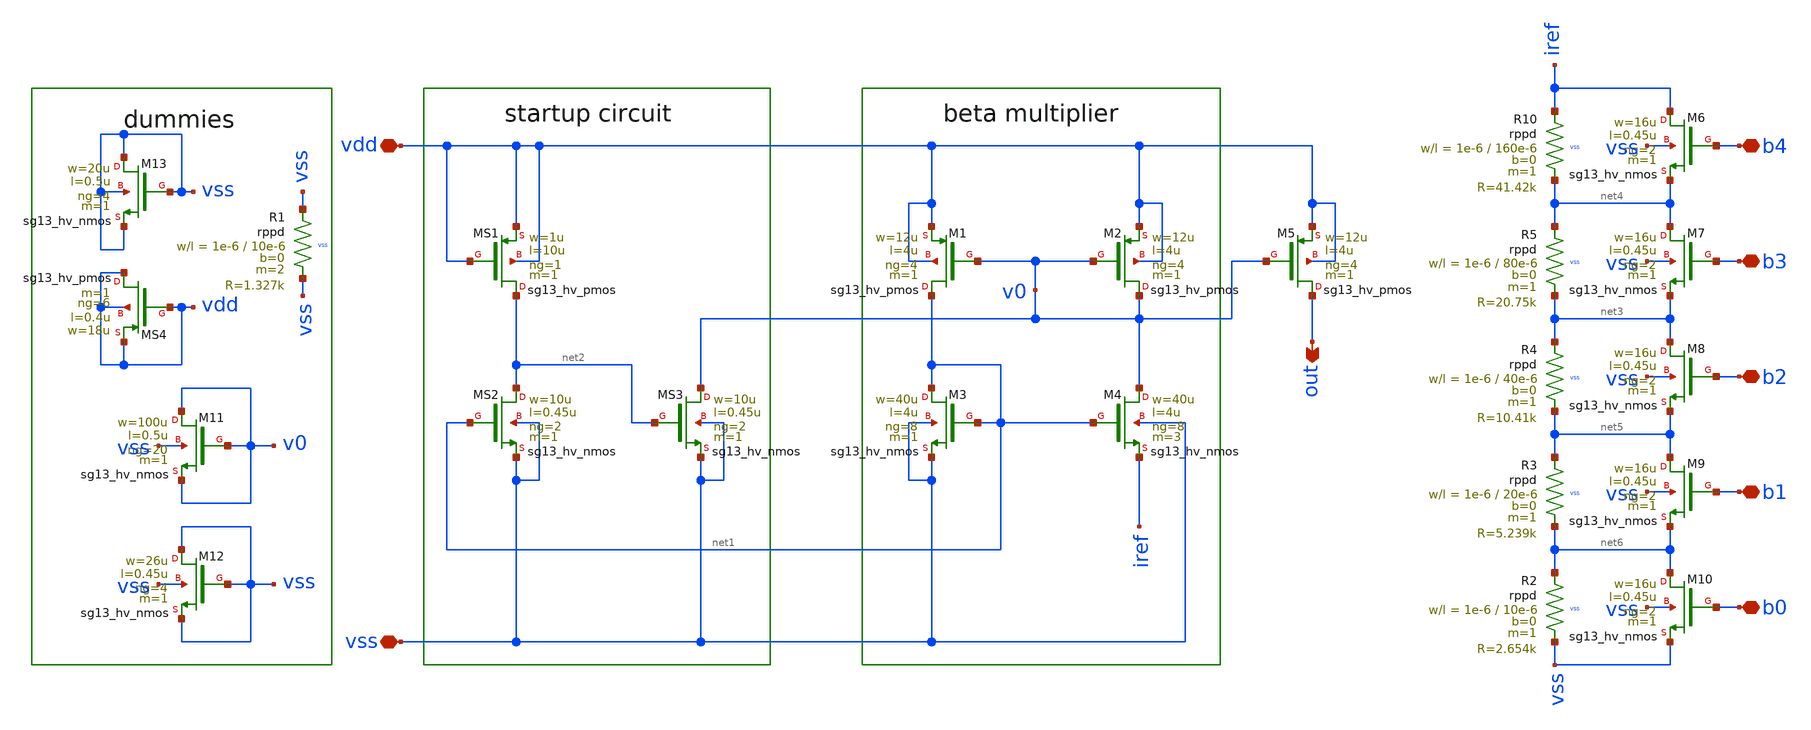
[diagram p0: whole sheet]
** sch_path: schematic/xschem/isource_beta.sch
**.subckt isource_beta out vdd vss b0 b1 b2 b3 b4
*.opin out
*.iopin vdd
*.iopin vss
*.iopin b0
*.iopin b1
*.iopin b2
*.iopin b3
*.iopin b4
XM1 net1 v0 vdd vdd sg13_hv_pmos w=12u l=4u ng=4 m=1 mm_ok=1
XM2 v0 v0 vdd vdd sg13_hv_pmos w=12u l=4u ng=4 m=1 mm_ok=1
XM3 net1 net1 vss vss sg13_hv_nmos w=40u l=4u ng=8 m=1 mm_ok=1
XM4 v0 net1 iref vss sg13_hv_nmos w=40u l=4u ng=8 m=3 mm_ok=1
XM5 out v0 vdd vdd sg13_hv_pmos w=12u l=4u ng=4 m=1 mm_ok=1
XMS1 net2 vdd vdd vdd sg13_hv_pmos w=1u l=10u ng=1 m=1 mm_ok=1
XMS2 net2 net1 vss vss sg13_hv_nmos w=10u l=0.45u ng=2 m=1 mm_ok=1
XMS3 v0 net2 vss vss sg13_hv_nmos w=10u l=0.45u ng=2 m=1 mm_ok=1
XR10 iref net4 vss rppd w=1e-6 l=160e-6 m=1 b=0 mm_ok=1
XR2 net6 vss vss rppd w=1e-6 l=10e-6 m=1 b=0 mm_ok=1
XM6 iref b4 net4 vss sg13_hv_nmos w=16u l=0.45u ng=2 m=1 mm_ok=1
XR3 net5 net6 vss rppd w=1e-6 l=20e-6 m=1 b=0 mm_ok=1
XR4 net3 net5 vss rppd w=1e-6 l=40e-6 m=1 b=0 mm_ok=1
XR5 net4 net3 vss rppd w=1e-6 l=80e-6 m=1 b=0 mm_ok=1
XM7 net4 b3 net3 vss sg13_hv_nmos w=16u l=0.45u ng=2 m=1 mm_ok=1
XM8 net3 b2 net5 vss sg13_hv_nmos w=16u l=0.45u ng=2 m=1 mm_ok=1
XM9 net5 b1 net6 vss sg13_hv_nmos w=16u l=0.45u ng=2 m=1 mm_ok=1
XM10 net6 b0 vss vss sg13_hv_nmos w=16u l=0.45u ng=2 m=1 mm_ok=1
XM11 v0 v0 v0 vss sg13_hv_nmos w=100u l=0.5u ng=20 m=1 mm_ok=1
XM12 vss vss vss vss sg13_hv_nmos w=26u l=0.45u ng=4 m=1 mm_ok=1
XR1 vss vss vss rppd w=1e-6 l=10e-6 m=2 b=0 mm_ok=1
XM13 vss vss vss vss sg13_hv_nmos w=20u l=0.5u ng=4 m=1 mm_ok=1
XMS4 vdd vdd vdd vdd sg13_hv_pmos w=18u l=0.4u ng=6 m=1 mm_ok=1
**.ends
.end
